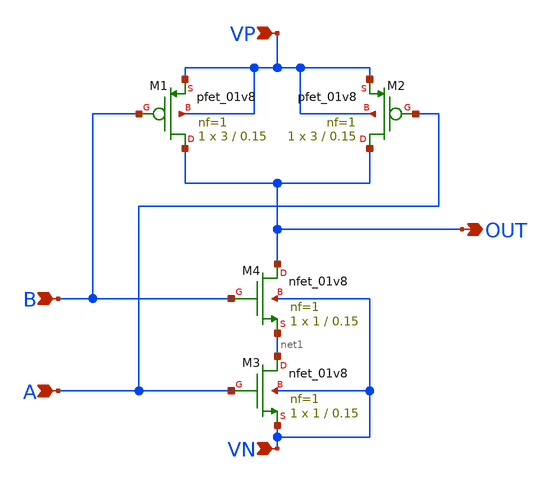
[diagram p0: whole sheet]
** sch_path: basic_cell/single_cell/nand/nand.sch
**.subckt nand A B OUT VN VP
*.ipin A
*.ipin B
*.opin OUT
*.ipin VN
*.ipin VP
XM4 OUT B net1 VN sky130_fd_pr__nfet_01v8 L=0.15 W=1 nf=1 ad='int((nf+1)/2) * W/nf * 0.29' as='int((nf+2)/2) * W/nf * 0.29'
+ pd='2*int((nf+1)/2) * (W/nf + 0.29)' ps='2*int((nf+2)/2) * (W/nf + 0.29)' nrd='0.29 / W' nrs='0.29 / W'
+ sa=0 sb=0 sd=0 mult=1 m=1
XM3 net1 A VN VN sky130_fd_pr__nfet_01v8 L=0.15 W=1 nf=1 ad='int((nf+1)/2) * W/nf * 0.29' as='int((nf+2)/2) * W/nf * 0.29'
+ pd='2*int((nf+1)/2) * (W/nf + 0.29)' ps='2*int((nf+2)/2) * (W/nf + 0.29)' nrd='0.29 / W' nrs='0.29 / W'
+ sa=0 sb=0 sd=0 mult=1 m=1
XM1 OUT B VP VP sky130_fd_pr__pfet_01v8 L=0.15 W=3 nf=1 ad='int((nf+1)/2) * W/nf * 0.29' as='int((nf+2)/2) * W/nf * 0.29'
+ pd='2*int((nf+1)/2) * (W/nf + 0.29)' ps='2*int((nf+2)/2) * (W/nf + 0.29)' nrd='0.29 / W' nrs='0.29 / W'
+ sa=0 sb=0 sd=0 mult=1 m=1
XM2 OUT A VP VP sky130_fd_pr__pfet_01v8 L=0.15 W=3 nf=1 ad='int((nf+1)/2) * W/nf * 0.29' as='int((nf+2)/2) * W/nf * 0.29'
+ pd='2*int((nf+1)/2) * (W/nf + 0.29)' ps='2*int((nf+2)/2) * (W/nf + 0.29)' nrd='0.29 / W' nrs='0.29 / W'
+ sa=0 sb=0 sd=0 mult=1 m=1
**.ends
.end
